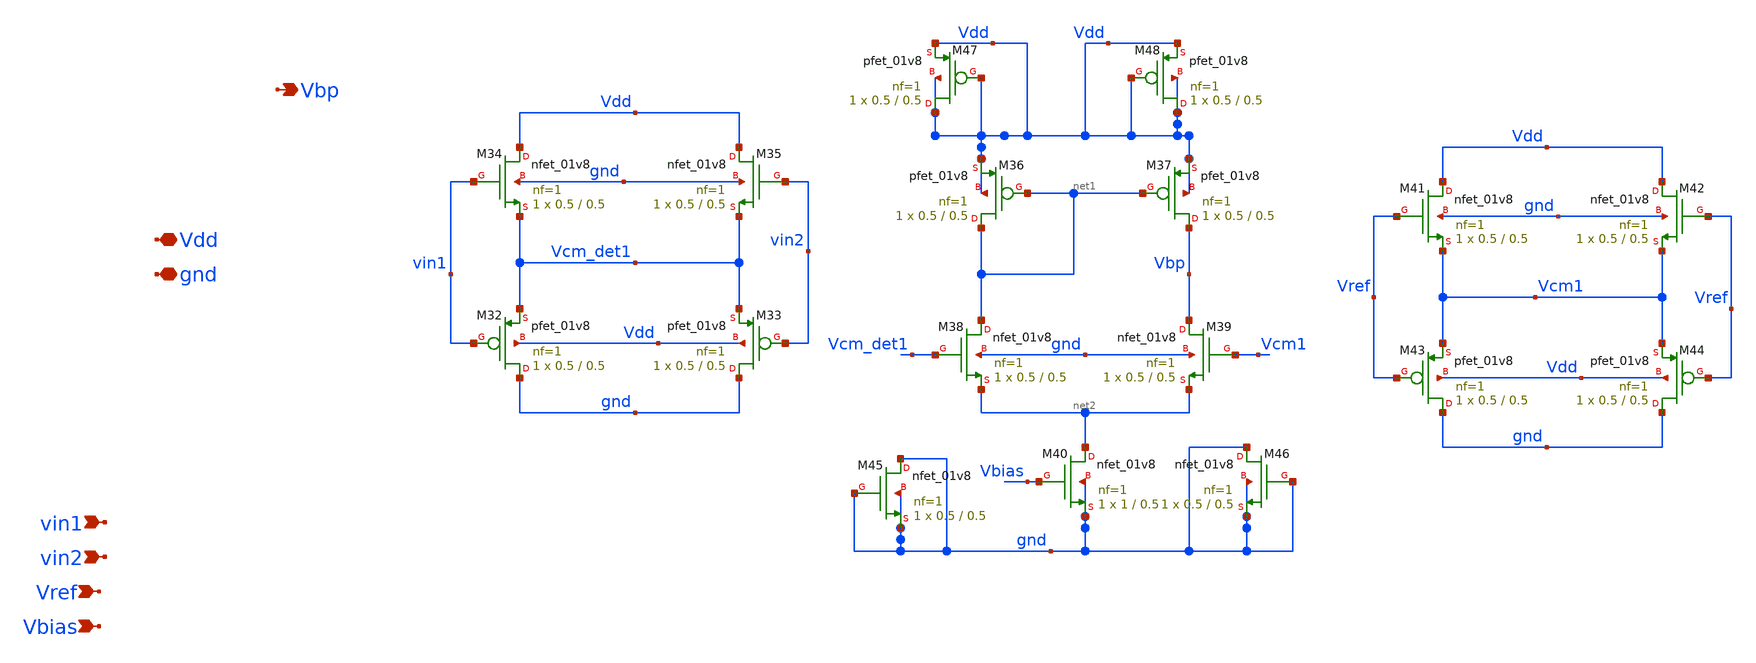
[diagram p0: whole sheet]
** sch_path: xschem/charge_pumps2/cmfb_lvs.sch
**.subckt cmfb_lvs vin1 vin2 Vref Vbias gnd Vdd Vbp
*.ipin vin1
*.ipin vin2
*.ipin Vref
*.ipin Vbias
*.iopin gnd
*.iopin Vdd
*.opin Vbp
XM32 gnd vin1 Vcm_det1 Vdd sky130_fd_pr__pfet_01v8 L=0.5 W=0.5 nf=1 ad='int((nf+1)/2) * W/nf * 0.29'
+ as='int((nf+2)/2) * W/nf * 0.29' pd='2*int((nf+1)/2) * (W/nf + 0.29)' ps='2*int((nf+2)/2) * (W/nf + 0.29)'
+ nrd='0.29 / W' nrs='0.29 / W' sa=0 sb=0 sd=0 mult=1 m=1
XM33 gnd vin2 Vcm_det1 Vdd sky130_fd_pr__pfet_01v8 L=0.5 W=0.5 nf=1 ad='int((nf+1)/2) * W/nf * 0.29'
+ as='int((nf+2)/2) * W/nf * 0.29' pd='2*int((nf+1)/2) * (W/nf + 0.29)' ps='2*int((nf+2)/2) * (W/nf + 0.29)'
+ nrd='0.29 / W' nrs='0.29 / W' sa=0 sb=0 sd=0 mult=1 m=1
XM34 Vdd vin1 Vcm_det1 gnd sky130_fd_pr__nfet_01v8 L=0.5 W=0.5 nf=1 ad='int((nf+1)/2) * W/nf * 0.29'
+ as='int((nf+2)/2) * W/nf * 0.29' pd='2*int((nf+1)/2) * (W/nf + 0.29)' ps='2*int((nf+2)/2) * (W/nf + 0.29)'
+ nrd='0.29 / W' nrs='0.29 / W' sa=0 sb=0 sd=0 mult=1 m=1
XM35 Vdd vin2 Vcm_det1 gnd sky130_fd_pr__nfet_01v8 L=0.5 W=0.5 nf=1 ad='int((nf+1)/2) * W/nf * 0.29'
+ as='int((nf+2)/2) * W/nf * 0.29' pd='2*int((nf+1)/2) * (W/nf + 0.29)' ps='2*int((nf+2)/2) * (W/nf + 0.29)'
+ nrd='0.29 / W' nrs='0.29 / W' sa=0 sb=0 sd=0 mult=1 m=1
XM36 net1 net1 Vdd Vdd sky130_fd_pr__pfet_01v8 L=0.5 W=0.5 nf=1 ad='int((nf+1)/2) * W/nf * 0.29' as='int((nf+2)/2) * W/nf * 0.29'
+ pd='2*int((nf+1)/2) * (W/nf + 0.29)' ps='2*int((nf+2)/2) * (W/nf + 0.29)' nrd='0.29 / W' nrs='0.29 / W'
+ sa=0 sb=0 sd=0 mult=1 m=1
XM37 Vbp net1 Vdd Vdd sky130_fd_pr__pfet_01v8 L=0.5 W=0.5 nf=1 ad='int((nf+1)/2) * W/nf * 0.29' as='int((nf+2)/2) * W/nf * 0.29'
+ pd='2*int((nf+1)/2) * (W/nf + 0.29)' ps='2*int((nf+2)/2) * (W/nf + 0.29)' nrd='0.29 / W' nrs='0.29 / W'
+ sa=0 sb=0 sd=0 mult=1 m=1
XM38 net1 Vcm_det1 net2 gnd sky130_fd_pr__nfet_01v8 L=0.5 W=0.5 nf=1 ad='int((nf+1)/2) * W/nf * 0.29'
+ as='int((nf+2)/2) * W/nf * 0.29' pd='2*int((nf+1)/2) * (W/nf + 0.29)' ps='2*int((nf+2)/2) * (W/nf + 0.29)'
+ nrd='0.29 / W' nrs='0.29 / W' sa=0 sb=0 sd=0 mult=1 m=1
XM39 Vbp Vcm1 net2 gnd sky130_fd_pr__nfet_01v8 L=0.5 W=0.5 nf=1 ad='int((nf+1)/2) * W/nf * 0.29' as='int((nf+2)/2) * W/nf * 0.29'
+ pd='2*int((nf+1)/2) * (W/nf + 0.29)' ps='2*int((nf+2)/2) * (W/nf + 0.29)' nrd='0.29 / W' nrs='0.29 / W'
+ sa=0 sb=0 sd=0 mult=1 m=1
XM40 net2 Vbias gnd gnd sky130_fd_pr__nfet_01v8 L=0.5 W=1 nf=1 ad='int((nf+1)/2) * W/nf * 0.29' as='int((nf+2)/2) * W/nf * 0.29'
+ pd='2*int((nf+1)/2) * (W/nf + 0.29)' ps='2*int((nf+2)/2) * (W/nf + 0.29)' nrd='0.29 / W' nrs='0.29 / W'
+ sa=0 sb=0 sd=0 mult=1 m=1
XM41 Vdd Vref Vcm1 gnd sky130_fd_pr__nfet_01v8 L=0.5 W=0.5 nf=1 ad='int((nf+1)/2) * W/nf * 0.29' as='int((nf+2)/2) * W/nf * 0.29'
+ pd='2*int((nf+1)/2) * (W/nf + 0.29)' ps='2*int((nf+2)/2) * (W/nf + 0.29)' nrd='0.29 / W' nrs='0.29 / W'
+ sa=0 sb=0 sd=0 mult=1 m=1
XM42 Vdd Vref Vcm1 gnd sky130_fd_pr__nfet_01v8 L=0.5 W=0.5 nf=1 ad='int((nf+1)/2) * W/nf * 0.29' as='int((nf+2)/2) * W/nf * 0.29'
+ pd='2*int((nf+1)/2) * (W/nf + 0.29)' ps='2*int((nf+2)/2) * (W/nf + 0.29)' nrd='0.29 / W' nrs='0.29 / W'
+ sa=0 sb=0 sd=0 mult=1 m=1
XM43 gnd Vref Vcm1 Vdd sky130_fd_pr__pfet_01v8 L=0.5 W=0.5 nf=1 ad='int((nf+1)/2) * W/nf * 0.29' as='int((nf+2)/2) * W/nf * 0.29'
+ pd='2*int((nf+1)/2) * (W/nf + 0.29)' ps='2*int((nf+2)/2) * (W/nf + 0.29)' nrd='0.29 / W' nrs='0.29 / W'
+ sa=0 sb=0 sd=0 mult=1 m=1
XM44 gnd Vref Vcm1 Vdd sky130_fd_pr__pfet_01v8 L=0.5 W=0.5 nf=1 ad='int((nf+1)/2) * W/nf * 0.29' as='int((nf+2)/2) * W/nf * 0.29'
+ pd='2*int((nf+1)/2) * (W/nf + 0.29)' ps='2*int((nf+2)/2) * (W/nf + 0.29)' nrd='0.29 / W' nrs='0.29 / W'
+ sa=0 sb=0 sd=0 mult=1 m=1
XM45 gnd gnd gnd gnd sky130_fd_pr__nfet_01v8 L=0.5 W=0.5 nf=1 ad='int((nf+1)/2) * W/nf * 0.29' as='int((nf+2)/2) * W/nf * 0.29'
+ pd='2*int((nf+1)/2) * (W/nf + 0.29)' ps='2*int((nf+2)/2) * (W/nf + 0.29)' nrd='0.29 / W' nrs='0.29 / W'
+ sa=0 sb=0 sd=0 mult=1 m=1
XM46 gnd gnd gnd gnd sky130_fd_pr__nfet_01v8 L=0.5 W=0.5 nf=1 ad='int((nf+1)/2) * W/nf * 0.29' as='int((nf+2)/2) * W/nf * 0.29'
+ pd='2*int((nf+1)/2) * (W/nf + 0.29)' ps='2*int((nf+2)/2) * (W/nf + 0.29)' nrd='0.29 / W' nrs='0.29 / W'
+ sa=0 sb=0 sd=0 mult=1 m=1
XM47 Vdd Vdd Vdd Vdd sky130_fd_pr__pfet_01v8 L=0.5 W=0.5 nf=1 ad='int((nf+1)/2) * W/nf * 0.29' as='int((nf+2)/2) * W/nf * 0.29'
+ pd='2*int((nf+1)/2) * (W/nf + 0.29)' ps='2*int((nf+2)/2) * (W/nf + 0.29)' nrd='0.29 / W' nrs='0.29 / W'
+ sa=0 sb=0 sd=0 mult=1 m=1
XM48 Vdd Vdd Vdd Vdd sky130_fd_pr__pfet_01v8 L=0.5 W=0.5 nf=1 ad='int((nf+1)/2) * W/nf * 0.29' as='int((nf+2)/2) * W/nf * 0.29'
+ pd='2*int((nf+1)/2) * (W/nf + 0.29)' ps='2*int((nf+2)/2) * (W/nf + 0.29)' nrd='0.29 / W' nrs='0.29 / W'
+ sa=0 sb=0 sd=0 mult=1 m=1
**.ends
.end
